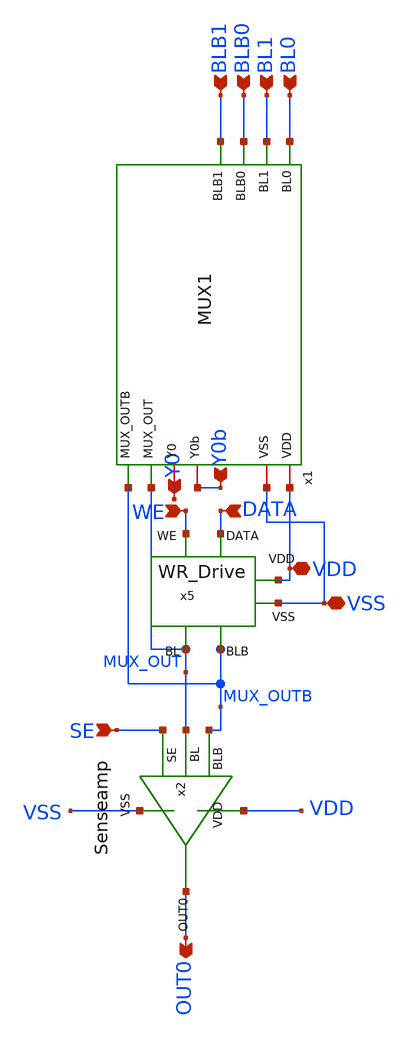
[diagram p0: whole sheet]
** sch_path: SRAM/combined_mux_sa_wrd/schematic/combined.sch
**.subckt combined BL0 BLB0 BL1 BLB1 DATA WE SE VDD VSS Y0 OUT0 Y0b
*.ipin BL0
*.ipin BLB0
*.ipin BL1
*.ipin BLB1
*.ipin DATA
*.ipin WE
*.ipin SE
*.iopin VDD
*.iopin VSS
*.ipin Y0
*.opin OUT0
*.ipin Y0b
x5 MUX_OUT MUX_OUTB WE VDD DATA VSS WR_Drive
x1 BL0 BLB0 BL1 BLB1 VDD VSS Y0 Y0b MUX_OUT MUX_OUTB MUX1
x2 VDD OUT0 MUX_OUTB MUX_OUT SE VSS Senseamp
**.ends

* expanding   symbol:  WR_Drive.sym # of pins=6
** sym_path: SRAM/wr_driver/schematic/WR_Drive.sym
** sch_path: SRAM/wr_driver/schematic/WR_Drive.sch
.subckt WR_Drive BL BLB WE VDD DATA VSS
*.ipin WE
*.ipin DATA
*.iopin VDD
*.iopin VSS
*.opin BL
*.opin BLB
M1 net1 WE VSS VSS nfet w=3.6u l=0.6u m=1
M4 net2 DATA VDD VDD pfet w=36u l=0.6u m=1
M5 net3 net2 VSS VSS nfet w=18u l=0.6u m=1
M6 net3 net2 VDD VDD pfet w=36u l=0.6u m=1
M7 net2 net1 BLB VDD pfet w=14.4u l=0.6u m=1
M8 BLB WE net2 VSS nfet w=7.2u l=0.6u m=1
M2 net1 WE VDD VDD pfet w=7.2u l=0.6u m=1
M3 net2 DATA VSS VSS nfet w=18u l=0.6u m=1
M9 BL WE net3 VSS nfet w=7.2u l=0.6u m=1
M10 net3 net1 BL VDD pfet w=14.4u l=0.6u m=1
.ends


* expanding   symbol:  MUX1.sym # of pins=10
** sym_path: SRAM/mux/schematic/MUX1.sym
** sch_path: SRAM/mux/schematic/MUX1.sch
.subckt MUX1 BL0 BLB0 BL1 BLB1 VDD VSS Y0 Y0b MUX_OUT MUX_OUTB
*.iopin BL0
*.iopin BLB0
*.iopin BL1
*.iopin BLB1
*.iopin VDD
*.iopin VSS
*.iopin Y0
*.iopin Y0b
*.opin MUX_OUT
*.opin MUX_OUTB
M1 BL0 Y0b MUX_OUT VDD pfet w=4.2u l=0.6u m=1
M2 BLB0 Y0b MUX_OUTB VDD pfet w=4.2u l=0.6u m=1
M3 BL1 Y0 MUX_OUT VDD pfet w=4.2u l=0.6u m=1
M4 BLB1 Y0 MUX_OUTB VDD pfet w=4.2u l=0.6u m=1
M5 BL0 Y0 MUX_OUT VSS nfet w=1.8u l=0.6u m=1
M6 BLB0 Y0 MUX_OUTB VSS nfet w=1.8u l=0.6u m=1
M7 BL1 Y0b MUX_OUT VSS nfet w=1.8u l=0.6u m=1
M8 BLB1 Y0b MUX_OUTB VSS nfet w=1.8u l=0.6u m=1
.ends


* expanding   symbol:  Senseamp.sym # of pins=6
** sym_path: SRAM/senseamp/schematic/Senseamp.sym
** sch_path: SRAM/senseamp/schematic/Senseamp.sch
.subckt Senseamp VDD OUT0 BLB BL SE VSS
*.ipin BLB
*.ipin BL
*.ipin SE
*.opin OUT0
*.iopin VSS
*.iopin VDD
M7 net2 net1 VDD VDD pfet w=3.6u l=0.6u m=1
M9 OUT0 net2 VDD VDD pfet w=3.6u l=0.6u m=1
M1 net1 BLB net3 VSS nfet w=1.2u l=0.6u m=1
M2 net3 SE VSS VSS nfet w=3.6u l=0.6u m=1
M3 net2 BL net3 VSS nfet w=1.2u l=0.6u m=1
M4 OUT0 SE VSS VSS nfet w=1.8u l=0.6u m=1
M5 net1 net1 VDD VDD pfet w=3.6u l=0.6u m=1
.ends

.end
